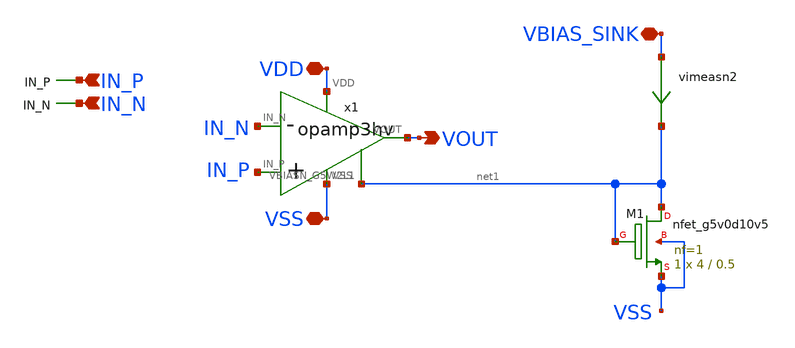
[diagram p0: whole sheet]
** sch_path: xschem/opamp3hvs.sch
**.subckt opamp3hvs IN_N IN_P VOUT VDD VSS VBIAS_SINK
*.ipin IN_N
*.ipin IN_P
*.opin VOUT
*.iopin VDD
*.iopin VSS
*.iopin VBIAS_SINK
XM1 net1 net1 VSS VSS sky130_fd_pr__nfet_g5v0d10v5 L=0.5 W=4 nf=1 ad='int((nf+1)/2) * W/nf * 0.29' as='int((nf+2)/2) * W/nf * 0.29'
+ pd='2*int((nf+1)/2) * (W/nf + 0.29)' ps='2*int((nf+2)/2) * (W/nf + 0.29)' nrd='0.29 / W' nrs='0.29 / W'
+ sa=0 sb=0 sd=0 mult=1 m=1
vimeasn2 VBIAS_SINK net1 0
.save i(vimeasn2)
x1 IN_N IN_P VOUT net1 VDD VSS opamp3hv
**.ends

* expanding   symbol:  opamp3hv.sym # of pins=6
** sym_path: xschem/opamp3hv.sym
** sch_path: xschem/opamp3hv.sch
.subckt opamp3hv IN_N IN_P VOUT VBIASN_G5W2L1 VDD VSS
*.iopin VDD
*.iopin VSS
*.ipin IN_N
*.opin VOUT
*.ipin IN_P
*.iopin VBIASN_G5W2L1
vimeasn net2 VN 0
.save i(vimeasn)
vimeasp net3 voutstage1 0
.save i(vimeasp)
vicom vcom net1 0
.save i(vicom)
XC1 VOUT voutstage1 sky130_fd_pr__cap_mim_m3_1 W=2 L=2 MF=1 m=1
XM6 net1 VBIASN_G5W2L1 VSS VSS sky130_fd_pr__nfet_g5v0d10v5 L=1 W=2 nf=1 ad='int((nf+1)/2) * W/nf * 0.29'
+ as='int((nf+2)/2) * W/nf * 0.29' pd='2*int((nf+1)/2) * (W/nf + 0.29)' ps='2*int((nf+2)/2) * (W/nf + 0.29)'
+ nrd='0.29 / W' nrs='0.29 / W' sa=0 sb=0 sd=0 mult=1 m=1
XM8 net3 net2 VDD VDD sky130_fd_pr__pfet_g5v0d10v5 L=1 W=2 nf=1 ad='int((nf+1)/2) * W/nf * 0.29' as='int((nf+2)/2) * W/nf * 0.29'
+ pd='2*int((nf+1)/2) * (W/nf + 0.29)' ps='2*int((nf+2)/2) * (W/nf + 0.29)' nrd='0.29 / W' nrs='0.29 / W'
+ sa=0 sb=0 sd=0 mult=1 m=1
XM2 net2 net2 VDD VDD sky130_fd_pr__pfet_g5v0d10v5 L=1 W=2 nf=1 ad='int((nf+1)/2) * W/nf * 0.29' as='int((nf+2)/2) * W/nf * 0.29'
+ pd='2*int((nf+1)/2) * (W/nf + 0.29)' ps='2*int((nf+2)/2) * (W/nf + 0.29)' nrd='0.29 / W' nrs='0.29 / W'
+ sa=0 sb=0 sd=0 mult=1 m=1
XM1 VOUT voutstage1 net4 VDD sky130_fd_pr__pfet_g5v0d10v5 L=0.5 W=16 nf=1 ad='int((nf+1)/2) * W/nf * 0.29'
+ as='int((nf+2)/2) * W/nf * 0.29' pd='2*int((nf+1)/2) * (W/nf + 0.29)' ps='2*int((nf+2)/2) * (W/nf + 0.29)'
+ nrd='0.29 / W' nrs='0.29 / W' sa=0 sb=0 sd=0 mult=2 m=2
XM4 net5 VBIASN_G5W2L1 VSS VSS sky130_fd_pr__nfet_g5v0d10v5 L=0.5 W=8 nf=1 ad='int((nf+1)/2) * W/nf * 0.29'
+ as='int((nf+2)/2) * W/nf * 0.29' pd='2*int((nf+1)/2) * (W/nf + 0.29)' ps='2*int((nf+2)/2) * (W/nf + 0.29)'
+ nrd='0.29 / W' nrs='0.29 / W' sa=0 sb=0 sd=0 mult=2 m=2
XM3 VN IN_N vcom VSS sky130_fd_pr__nfet_03v3_nvt L=0.5 W=4 nf=1 ad='int((nf+1)/2) * W/nf * 0.29' as='int((nf+2)/2) * W/nf * 0.29'
+ pd='2*int((nf+1)/2) * (W/nf + 0.29)' ps='2*int((nf+2)/2) * (W/nf + 0.29)' nrd='0.29 / W' nrs='0.29 / W'
+ sa=0 sb=0 sd=0 mult=4 m=4
XM5 voutstage1 IN_P vcom VSS sky130_fd_pr__nfet_03v3_nvt L=0.5 W=4 nf=1 ad='int((nf+1)/2) * W/nf * 0.29'
+ as='int((nf+2)/2) * W/nf * 0.29' pd='2*int((nf+1)/2) * (W/nf + 0.29)' ps='2*int((nf+2)/2) * (W/nf + 0.29)'
+ nrd='0.29 / W' nrs='0.29 / W' sa=0 sb=0 sd=0 mult=4 m=4
XC2 VDD VSS sky130_fd_pr__cap_mim_m3_1 W=4 L=4 MF=1 m=1
vimeasp1 VDD net4 0
.save i(vimeasp1)
vimeasn1 VOUT net5 0
.save i(vimeasn1)
.ends

.end
